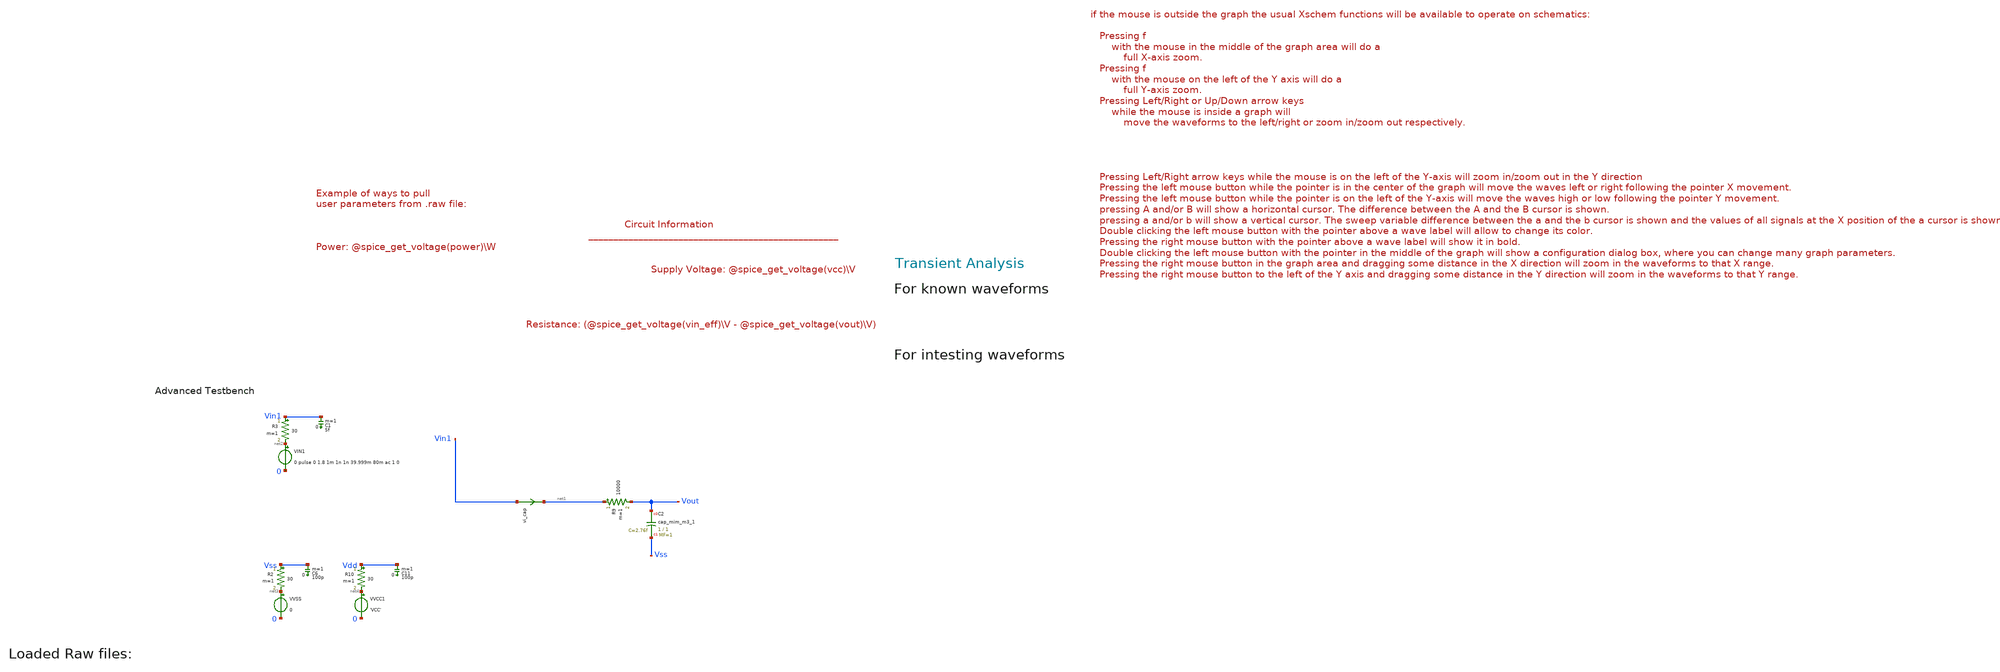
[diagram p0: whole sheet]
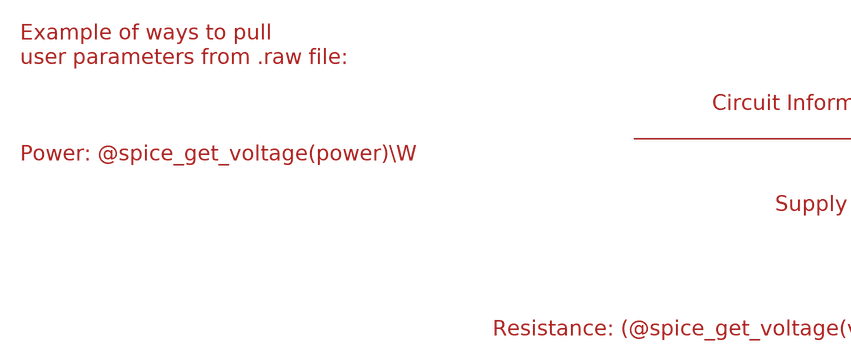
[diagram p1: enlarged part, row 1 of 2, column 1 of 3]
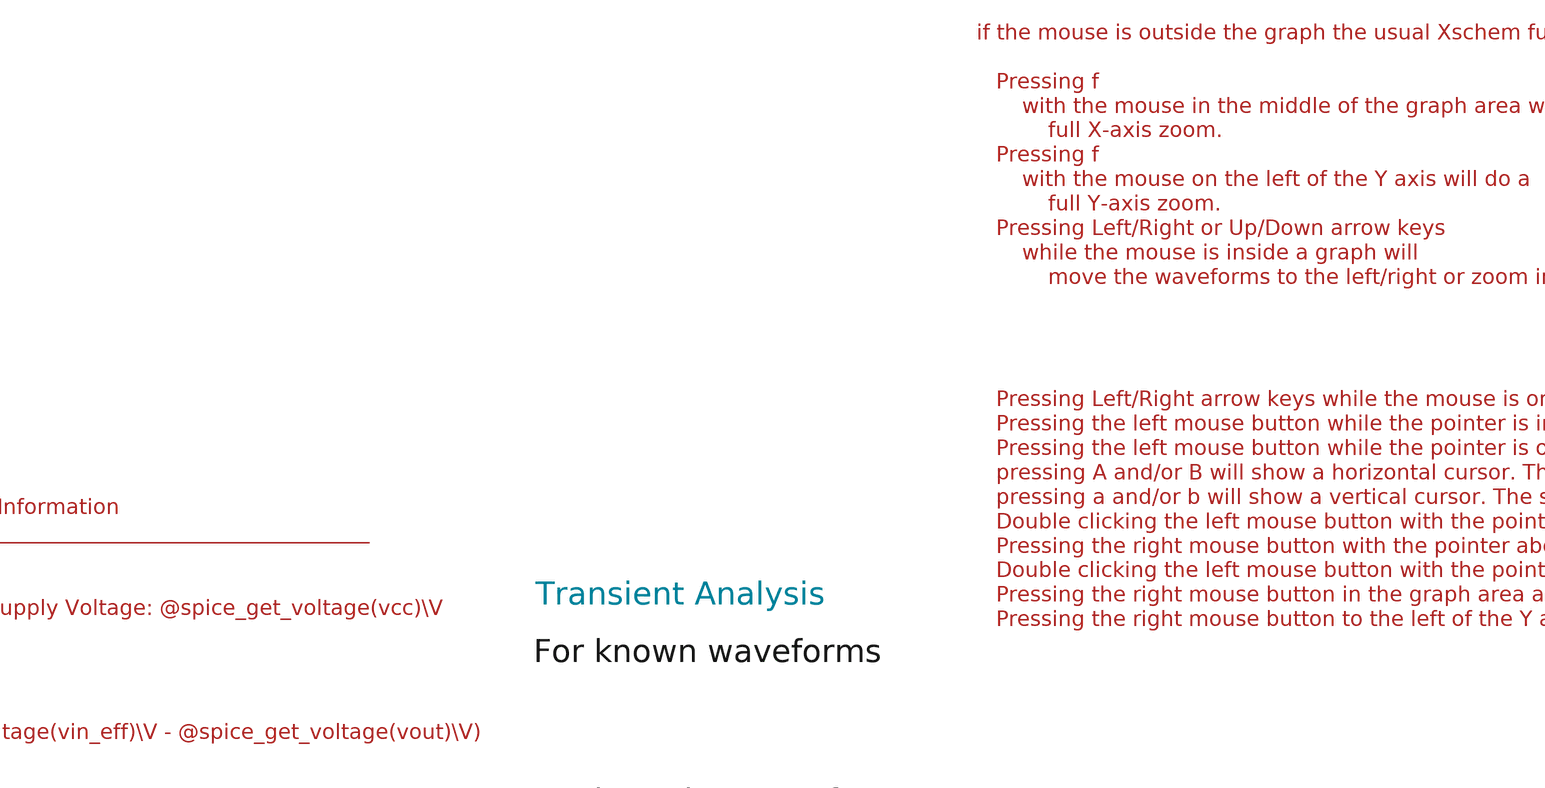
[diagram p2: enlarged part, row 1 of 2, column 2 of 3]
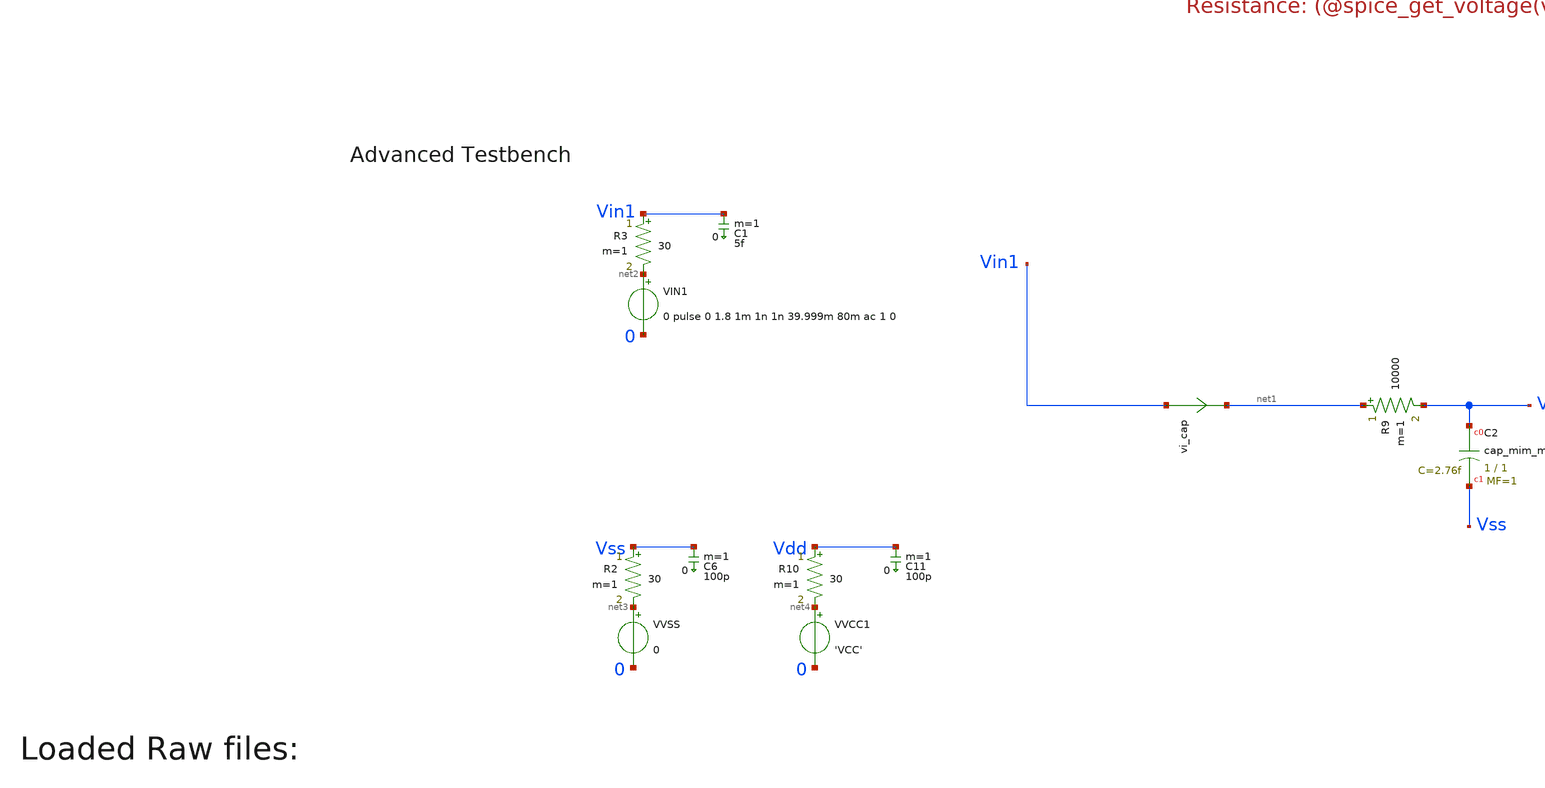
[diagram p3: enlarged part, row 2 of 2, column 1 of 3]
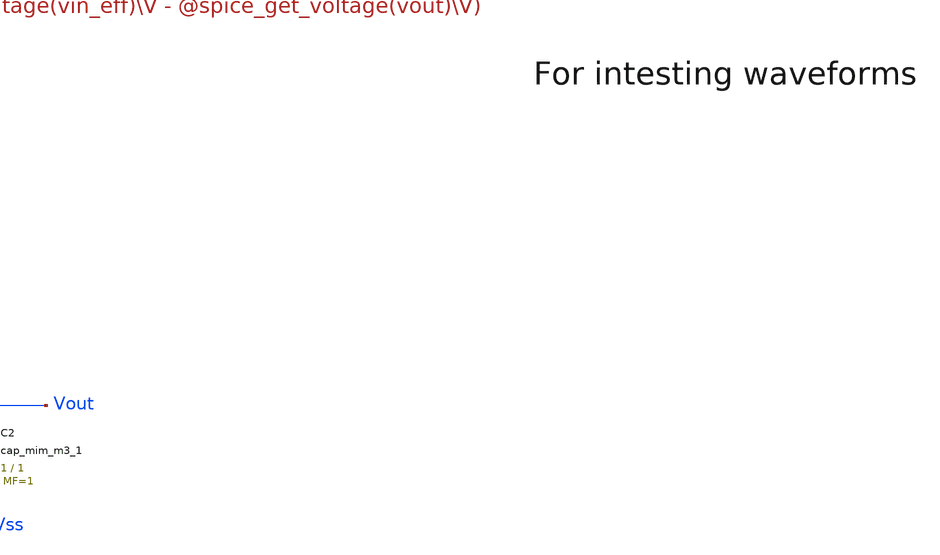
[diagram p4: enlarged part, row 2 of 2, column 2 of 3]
** sch_path: tt10-hdl/tt_um_test_commit/xschem/T0/RC/RC_tb.sch
* Copyright (C) 1998-2024 Stefan Frederik Schippers
* This program is free software; you can redistribute it and/or modify
* it under the terms of the GNU General Public License as published by
* the Free Software Foundation; either version 2 of the License, or
* (at your option) any later version.
* This program is distributed in the hope that it will be useful,
* but WITHOUT ANY WARRANTY; without even the implied warranty of
* MERCHANTABILITY or FITNESS FOR A PARTICULAR PURPOSE.  See the
* GNU General Public License for more details.
* You should have received a copy of the GNU General Public License
* along with this program; if not, write to the Free Software
**.subckt RC_tb
VIN1 net2 0 0 pulse 0 1.8 1m 1n 1n 39.999m 80m ac 1 0
R9 net1 Vout 10000 m=1
vi_cap Vin1 net1 0
.save i(vi_cap)
VVSS net3 0 0
R2 Vss net3 30 m=1
C6 Vss 0 100p m=1
VVCC1 net4 0 'VCC'
R10 Vdd net4 30 m=1
C11 Vdd 0 100p m=1
R3 Vin1 net2 30 m=1
C1 Vin1 0 5f m=1
XC2 Vout Vss sky130_fd_pr__cap_mim_m3_1 W=1 L=1 MF=1 m=1
**** begin user architecture code



.temp 30
*.param IB=1n
.param VCC = 1.8

.option savecurrents
.save all @m1[gm]
.control
  save all alli
  op
  let power=-v(vcc) * i(vvcc)
  settype power power
  write template_adv_tb.raw
  set appendwrite

  *dc vin1 0 1.8 0.001
  *write template_adv_tb.raw

  tran 1u 2m
  *tran 0.01n 15n
  write template_adv_tb.raw

  *ac dec 10 1 1G
  *remzerovec
  *write template_adv_tb.raw



  quit 0




.endc





** opencircuitdesign pdks install
.lib $::SKYWATER_MODELS/sky130.lib.spice tt


**** end user architecture code
**.ends
.end
